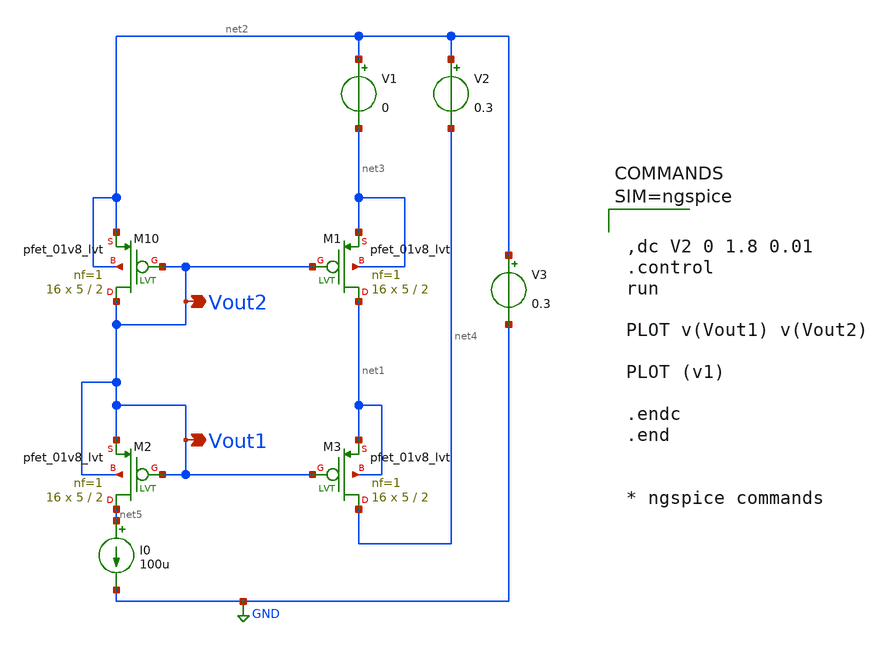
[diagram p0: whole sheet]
** sch_path: spice/cascode_pmos.sch
**.subckt cascode_pmos Vout1 Vout2
*.opin Vout1
*.opin Vout2
XM10 Vout1 Vout1 net2 net2 sky130_fd_pr__pfet_01v8_lvt L=2 W=5 nf=1 ad='int((1 + 1)/2) * 5 / 1 * 0.29'
+ as='int((1 + 2)/2) * 5 / 1 * 0.29' pd='2*int((1 + 1)/2) * (5 / 1 + 0.29)' ps='2*int((1 + 2)/2) * (5 / 1 + 0.29)'
+ nrd='0.29 / 5 ' nrs='0.29 / 5 ' sa=0 sb=0 sd=0 mult=16 m=16
XM1 net1 Vout1 net3 net3 sky130_fd_pr__pfet_01v8_lvt L=2 W=5 nf=1 ad='int((1 + 1)/2) * 5 / 1 * 0.29'
+ as='int((1 + 2)/2) * 5 / 1 * 0.29' pd='2*int((1 + 1)/2) * (5 / 1 + 0.29)' ps='2*int((1 + 2)/2) * (5 / 1 + 0.29)'
+ nrd='0.29 / 5 ' nrs='0.29 / 5 ' sa=0 sb=0 sd=0 mult=16 m=16
XM2 net5 Vout1 Vout1 Vout1 sky130_fd_pr__pfet_01v8_lvt L=2 W=5 nf=1 ad='int((1 + 1)/2) * 5 / 1 * 0.29'
+ as='int((1 + 2)/2) * 5 / 1 * 0.29' pd='2*int((1 + 1)/2) * (5 / 1 + 0.29)' ps='2*int((1 + 2)/2) * (5 / 1 + 0.29)'
+ nrd='0.29 / 5 ' nrs='0.29 / 5 ' sa=0 sb=0 sd=0 mult=16 m=16
XM3 net4 Vout1 net1 net1 sky130_fd_pr__pfet_01v8_lvt L=2 W=5 nf=1 ad='int((1 + 1)/2) * 5 / 1 * 0.29'
+ as='int((1 + 2)/2) * 5 / 1 * 0.29' pd='2*int((1 + 1)/2) * (5 / 1 + 0.29)' ps='2*int((1 + 2)/2) * (5 / 1 + 0.29)'
+ nrd='0.29 / 5 ' nrs='0.29 / 5 ' sa=0 sb=0 sd=0 mult=16 m=16
V1 net2 net3 0
V2 net2 net4 0.3
V3 net2 GND 0.3
I0 net5 GND 100u
**** begin user architecture code



,dc V2 0 1.8 0.01
.control
run

PLOT v(Vout1) v(Vout2)

PLOT (v1)

.endc
.end


* ngspice commands




** opencircuitdesign pdks install
.lib $::SKYWATER_MODELS/sky130.lib.spice tt

**** end user architecture code
**.ends
.GLOBAL GND
.end
